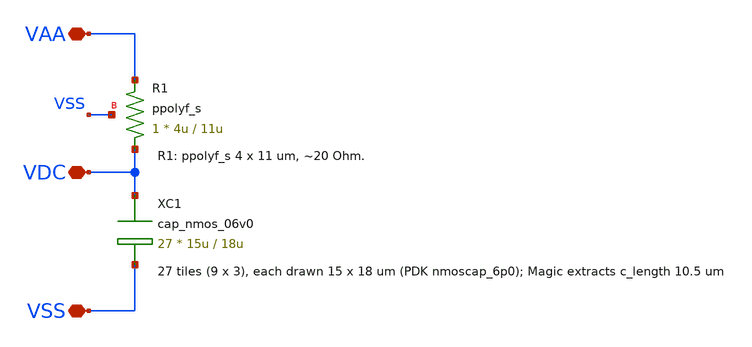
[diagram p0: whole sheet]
** sch_path: xschem/dcap_lump.sch
**.subckt dcap_lump VAA VSS VDC
*.iopin VAA
*.iopin VSS
*.iopin VDC
XR1 VDC VAA VSS ppolyf_s r_width=4u r_length=11u m=1
XC1 VDC VSS cap_nmos_06v0 c_width=15u c_length=18u m=27
**.ends
.end
